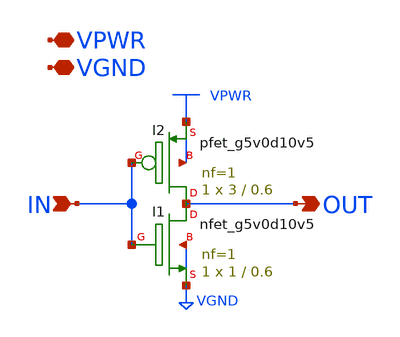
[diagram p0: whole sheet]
** sch_path: com_inv_x1_dnw.sch
* Copyright 2023 David Mitchell Bailey
* Licensed under the Apache License, Version 2.0 (the "License");
* you may not use this file except in compliance with the License.
* You may obtain a copy of the License at
* https://www.apache.org/licenses/LICENSE-2.0
* Unless required by applicable law or agreed to in writing, software
* distributed under the License is distributed on an "AS IS" BASIS,
* WITHOUT WARRANTIES OR CONDITIONS OF ANY KIND, either express or implied.
* See the License for the specific language governing permissions and
* limitations under the License.
**.subckt com_inv_x1_dnw IN OUT VPWR VGND
*.ipin IN
*.opin OUT
*.iopin VPWR
*.iopin VGND
XI1 OUT IN VGND VGND sky130_fd_pr__nfet_g5v0d10v5 L=0.6 W=1 nf=1 ad='int((nf+1)/2) * W/nf * 0.29' as='int((nf+2)/2) * W/nf * 0.29'
+ pd='2*int((nf+1)/2) * (W/nf + 0.29)' ps='2*int((nf+2)/2) * (W/nf + 0.29)' nrd='0.29 / W' nrs='0.29 / W'
+ sa=0 sb=0 sd=0 mult=1 m=1
XI2 OUT IN VPWR VPWR sky130_fd_pr__pfet_g5v0d10v5 L=0.6 W=3 nf=1 ad='int((nf+1)/2) * W/nf * 0.29' as='int((nf+2)/2) * W/nf * 0.29'
+ pd='2*int((nf+1)/2) * (W/nf + 0.29)' ps='2*int((nf+2)/2) * (W/nf + 0.29)' nrd='0.29 / W' nrs='0.29 / W'
+ sa=0 sb=0 sd=0 mult=1 m=1
**.ends
.end
